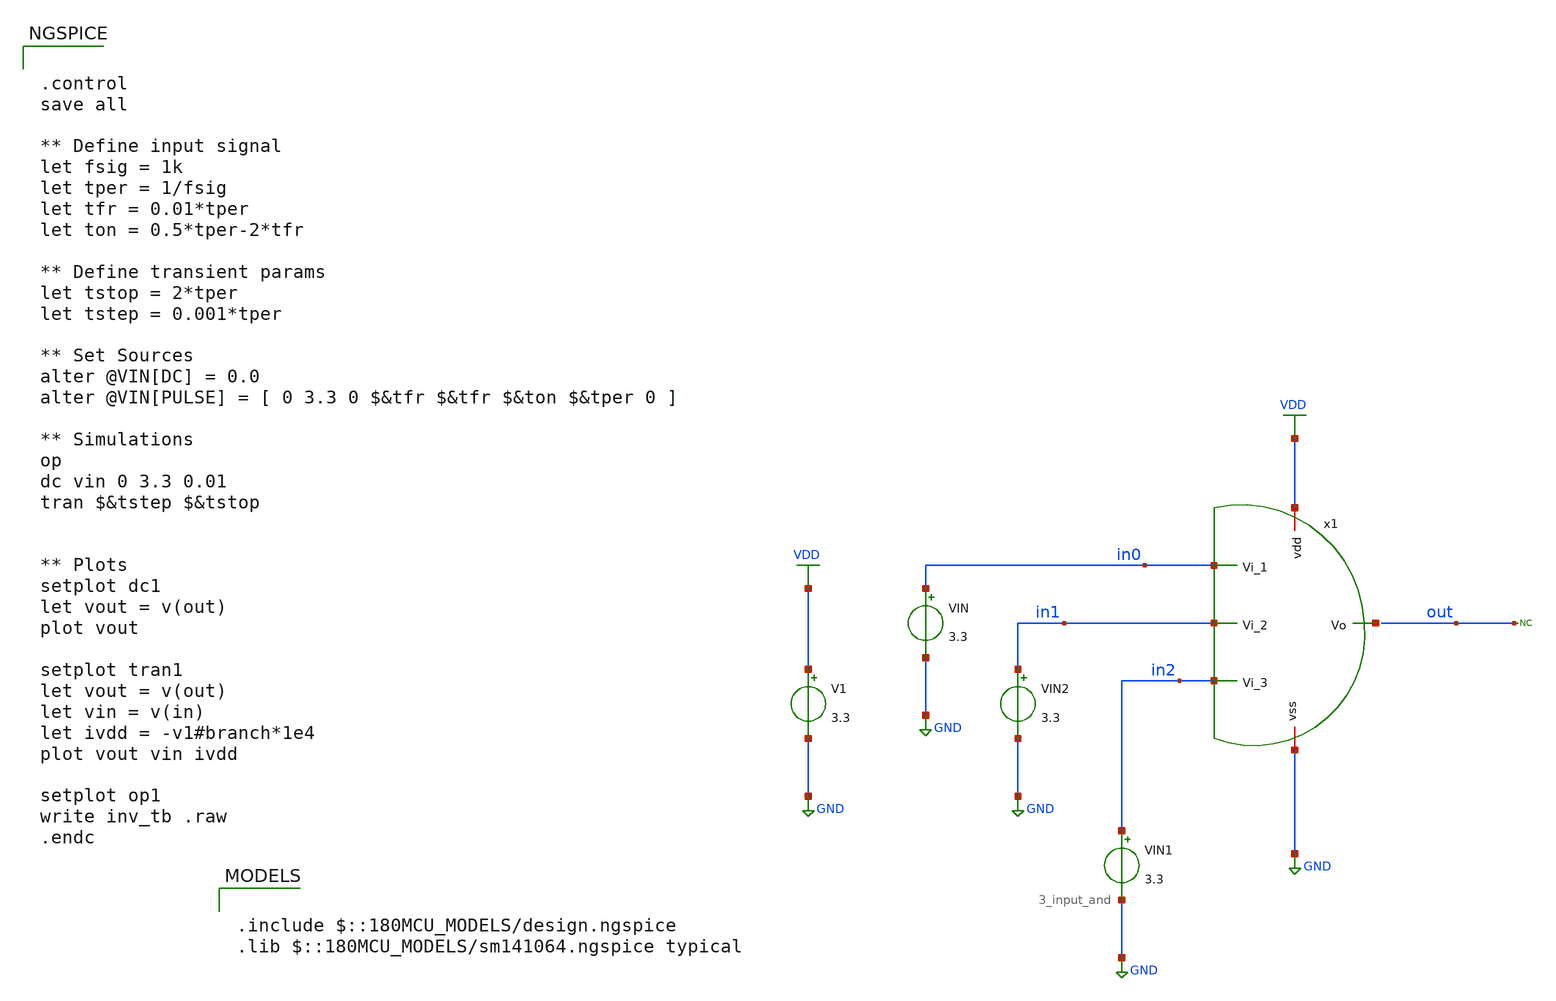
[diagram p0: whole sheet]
** sch_path: designs/untitled.sch
**.subckt untitled
x1 VDD net1 in0 in1 in2 GND 3_input_and
V1 VDD GND 3.3
VIN in0 GND 3.3
* noconn out
VIN1 in2 GND 3.3
VIN2 in1 GND 3.3
**** begin user architecture code

.include $::180MCU_MODELS/design.ngspice
.lib $::180MCU_MODELS/sm141064.ngspice typical



.control
save all

** Define input signal
let fsig = 1k
let tper = 1/fsig
let tfr = 0.01*tper
let ton = 0.5*tper-2*tfr

** Define transient params
let tstop = 2*tper
let tstep = 0.001*tper

** Set Sources
alter @VIN[DC] = 0.0
alter @VIN[PULSE] = [ 0 3.3 0 $&tfr $&tfr $&ton $&tper 0 ]

** Simulations
op
dc vin 0 3.3 0.01
tran $&tstep $&tstop


** Plots
setplot dc1
let vout = v(out)
plot vout

setplot tran1
let vout = v(out)
let vin = v(in)
let ivdd = -v1#branch*1e4
plot vout vin ivdd

setplot op1
write inv_tb .raw
.endc


**** end user architecture code
**.ends

* expanding   symbol:  3_input_and.sym # of pins=6
** sym_path: designs/3_input_and.sym
** sch_path: designs/3_input_and.sch
.subckt 3_input_and vdd Vo Vi_1 Vi_2 Vi_3 vss
*.iopin vdd
*.iopin vss
*.ipin Vi_1
*.ipin Vi_2
*.ipin Vi_3
*.opin Vo
XM1 net1 Vi_1 vdd vdd pfet_03v3 L=0.28u W=0.22u nf=1 ad='int((nf+1)/2) * W/nf * 0.18u' as='int((nf+2)/2) * W/nf * 0.18u'
+ pd='2*int((nf+1)/2) * (W/nf + 0.18u)' ps='2*int((nf+2)/2) * (W/nf + 0.18u)' nrd='0.18u / W' nrs='0.18u / W'
+ sa=0 sb=0 sd=0 m=1
XM2 net1 Vi_2 vdd vdd pfet_03v3 L=0.28u W=0.22u nf=1 ad='int((nf+1)/2) * W/nf * 0.18u' as='int((nf+2)/2) * W/nf * 0.18u'
+ pd='2*int((nf+1)/2) * (W/nf + 0.18u)' ps='2*int((nf+2)/2) * (W/nf + 0.18u)' nrd='0.18u / W' nrs='0.18u / W'
+ sa=0 sb=0 sd=0 m=1
XM3 net1 Vi_3 vdd vdd pfet_03v3 L=0.28u W=0.22u nf=1 ad='int((nf+1)/2) * W/nf * 0.18u' as='int((nf+2)/2) * W/nf * 0.18u'
+ pd='2*int((nf+1)/2) * (W/nf + 0.18u)' ps='2*int((nf+2)/2) * (W/nf + 0.18u)' nrd='0.18u / W' nrs='0.18u / W'
+ sa=0 sb=0 sd=0 m=1
XM4 net1 Vi_1 net3 vss nfet_03v3 L=0.28u W=0.22u nf=1 ad='int((nf+1)/2) * W/nf * 0.18u' as='int((nf+2)/2) * W/nf * 0.18u'
+ pd='2*int((nf+1)/2) * (W/nf + 0.18u)' ps='2*int((nf+2)/2) * (W/nf + 0.18u)' nrd='0.18u / W' nrs='0.18u / W'
+ sa=0 sb=0 sd=0 m=1
XM5 net3 Vi_2 net2 vss nfet_03v3 L=0.28u W=0.22u nf=1 ad='int((nf+1)/2) * W/nf * 0.18u' as='int((nf+2)/2) * W/nf * 0.18u'
+ pd='2*int((nf+1)/2) * (W/nf + 0.18u)' ps='2*int((nf+2)/2) * (W/nf + 0.18u)' nrd='0.18u / W' nrs='0.18u / W'
+ sa=0 sb=0 sd=0 m=1
XM6 net2 Vi_3 vss vss nfet_03v3 L=0.28u W=0.22u nf=1 ad='int((nf+1)/2) * W/nf * 0.18u' as='int((nf+2)/2) * W/nf * 0.18u'
+ pd='2*int((nf+1)/2) * (W/nf + 0.18u)' ps='2*int((nf+2)/2) * (W/nf + 0.18u)' nrd='0.18u / W' nrs='0.18u / W'
+ sa=0 sb=0 sd=0 m=1
XM7 Vo net1 vdd vdd pfet_03v3 L=0.28u W=0.22u nf=1 ad='int((nf+1)/2) * W/nf * 0.18u' as='int((nf+2)/2) * W/nf * 0.18u'
+ pd='2*int((nf+1)/2) * (W/nf + 0.18u)' ps='2*int((nf+2)/2) * (W/nf + 0.18u)' nrd='0.18u / W' nrs='0.18u / W'
+ sa=0 sb=0 sd=0 m=1
XM8 Vo net1 vss vss nfet_03v3 L=0.28u W=0.22u nf=1 ad='int((nf+1)/2) * W/nf * 0.18u' as='int((nf+2)/2) * W/nf * 0.18u'
+ pd='2*int((nf+1)/2) * (W/nf + 0.18u)' ps='2*int((nf+2)/2) * (W/nf + 0.18u)' nrd='0.18u / W' nrs='0.18u / W'
+ sa=0 sb=0 sd=0 m=1
.ends

.GLOBAL VDD
.GLOBAL GND
.end
